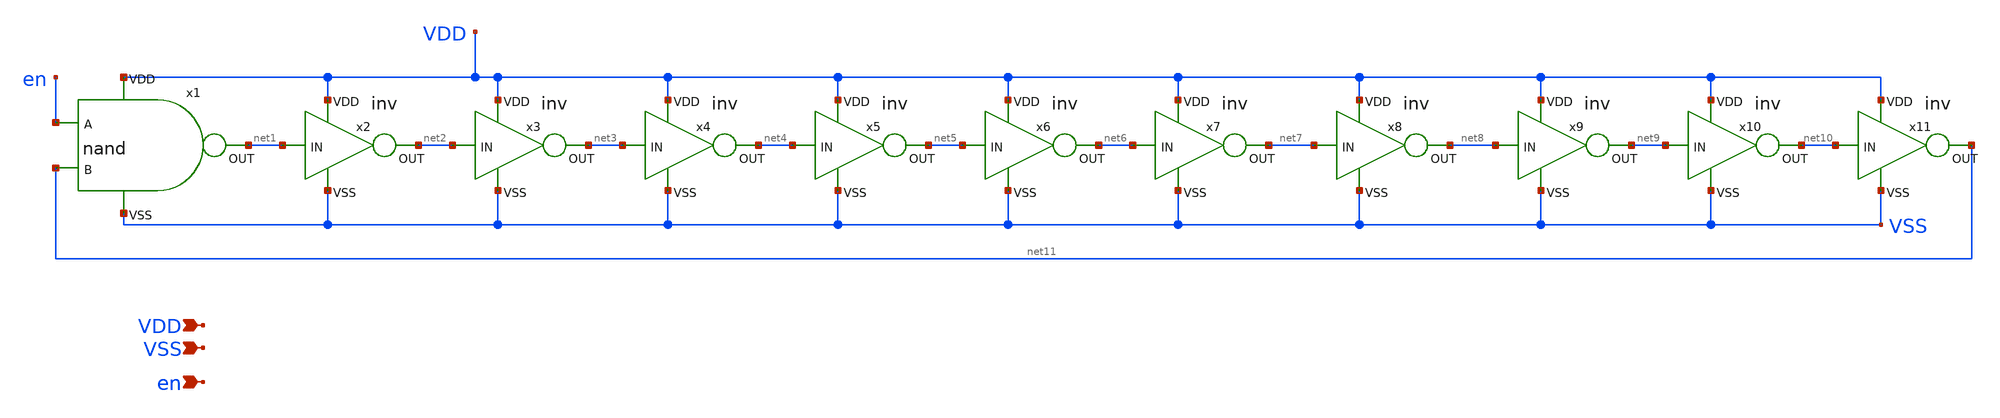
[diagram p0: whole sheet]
** sch_path: test_RO/RO/RO.sch
**.subckt RO en en VSS VDD
*.ipin en
*.ipin en
*.ipin VSS
*.ipin VDD
x1 en net11 net1 VDD VSS nand
x2 VDD VSS net1 net2 inv
x3 VDD VSS net2 net3 inv
x4 VDD VSS net3 net4 inv
x5 VDD VSS net4 net5 inv
x6 VDD VSS net5 net6 inv
x7 VDD VSS net6 net7 inv
x8 VDD VSS net7 net8 inv
x9 VDD VSS net8 net9 inv
x10 VDD VSS net9 net10 inv
x11 VDD VSS net10 net11 inv
**.ends
.end
